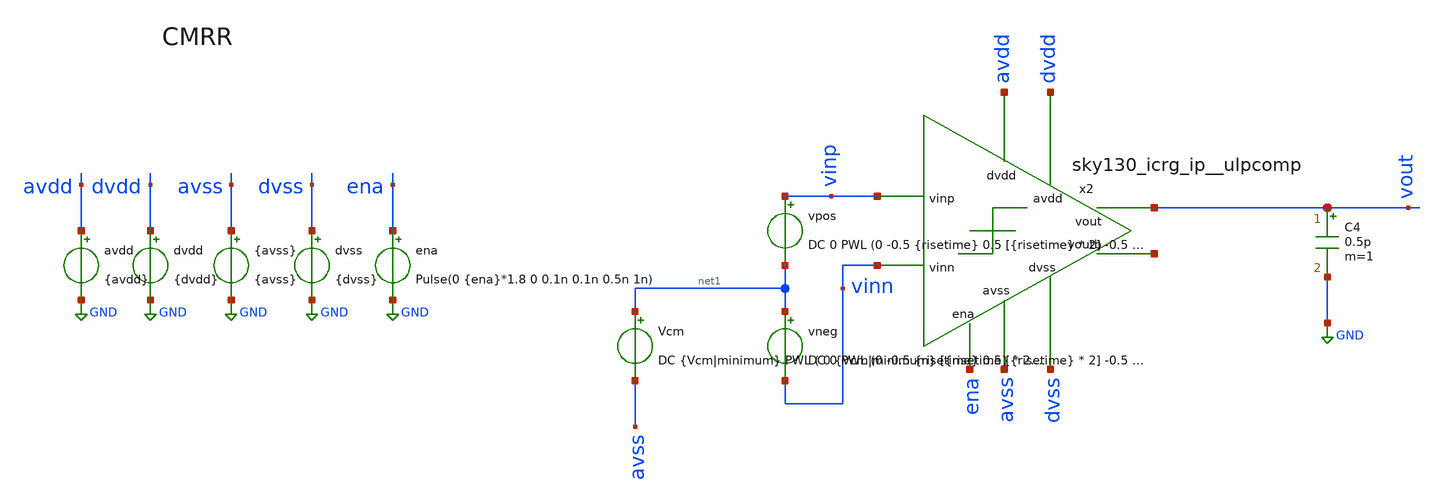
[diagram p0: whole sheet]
** sch_path: cace/tb_CMRR.sch
**.subckt tb_CMRR
x2 avdd dvdd ena vinp vinn vout net2 avss dvss sky130_icrg_ip__ulpcomp
vpos vinp net1 DC 0 PWL (0 -0.5 {risetime} 0.5 [{risetime} * 2] -0.5 [{risetime} * 3] 0.5 [{risetime}
+ * 4] -0.5 )
avdd avdd GND {avdd}
dvdd dvdd GND {dvdd}
{avss} avss GND {avss}
dvss dvss GND {dvss}
C4 vout GND 0.5p m=1
Vcm net1 avss DC {Vcm|minimum} PWL ( 0 {Vcm|minimum} [{risetime} * 2] {Vcm|minimum} [{risetime} * 2 +
+ 1e-9] {Vcm|maximum} [{risetime} * 3] {Vcm|maximum} )
ena ena GND Pulse(0 {ena}*1.8 0 0.1n 0.1n 0.5n 1n)
vneg net1 vinn DC 0 PWL (0 -0.5 {risetime} 0.5 [{risetime} * 2] -0.5 [{risetime} * 3] 0.5 [{risetime}
+ * 4] -0.5 )
**** begin user architecture code


.lib /home/ttuser/pdk/sky130A/libs.tech/combined/sky130.lib.spice {corner}
.option TEMP={temperature}


.control
** CMRR is defined as the change in input offset vs. change in common-mode voltage.
tran [{risetime} * 2 / 100] [{risetime} * 4]
meas tran vhigh1 FIND V(vinp) WHEN V(vout) = [{dvdd} / 2] CROSS=1
meas tran vlow1 FIND V(vinp) WHEN V(vout) = [{dvdd} / 2] CROSS=2
meas tran vhigh2 FIND V(vinp) WHEN V(vout) = [{dvdd} / 2] CROSS=3
meas tran vlow2 FIND V(vinp) WHEN V(vout) = [{dvdd} / 2] CROSS=4

let voffset1 = 0.5 * ($&vhigh1 + $&vlow1) - {Vcm|minimum}
let voffset2 = 0.5 * ($&vhigh2 + $&vlow2) - {Vcm|maximum}

let cmrr = ($&voffset1 - $&voffset2) / ({Vcm|maximum} - {Vcm|minimum})
let cmrrdb = 20 * log(abs($&cmrr))

echo $&cmrrdb > {simpath}/{filename}_{N}.data
quit
.endc


**** end user architecture code
**.ends
.GLOBAL GND
.end
